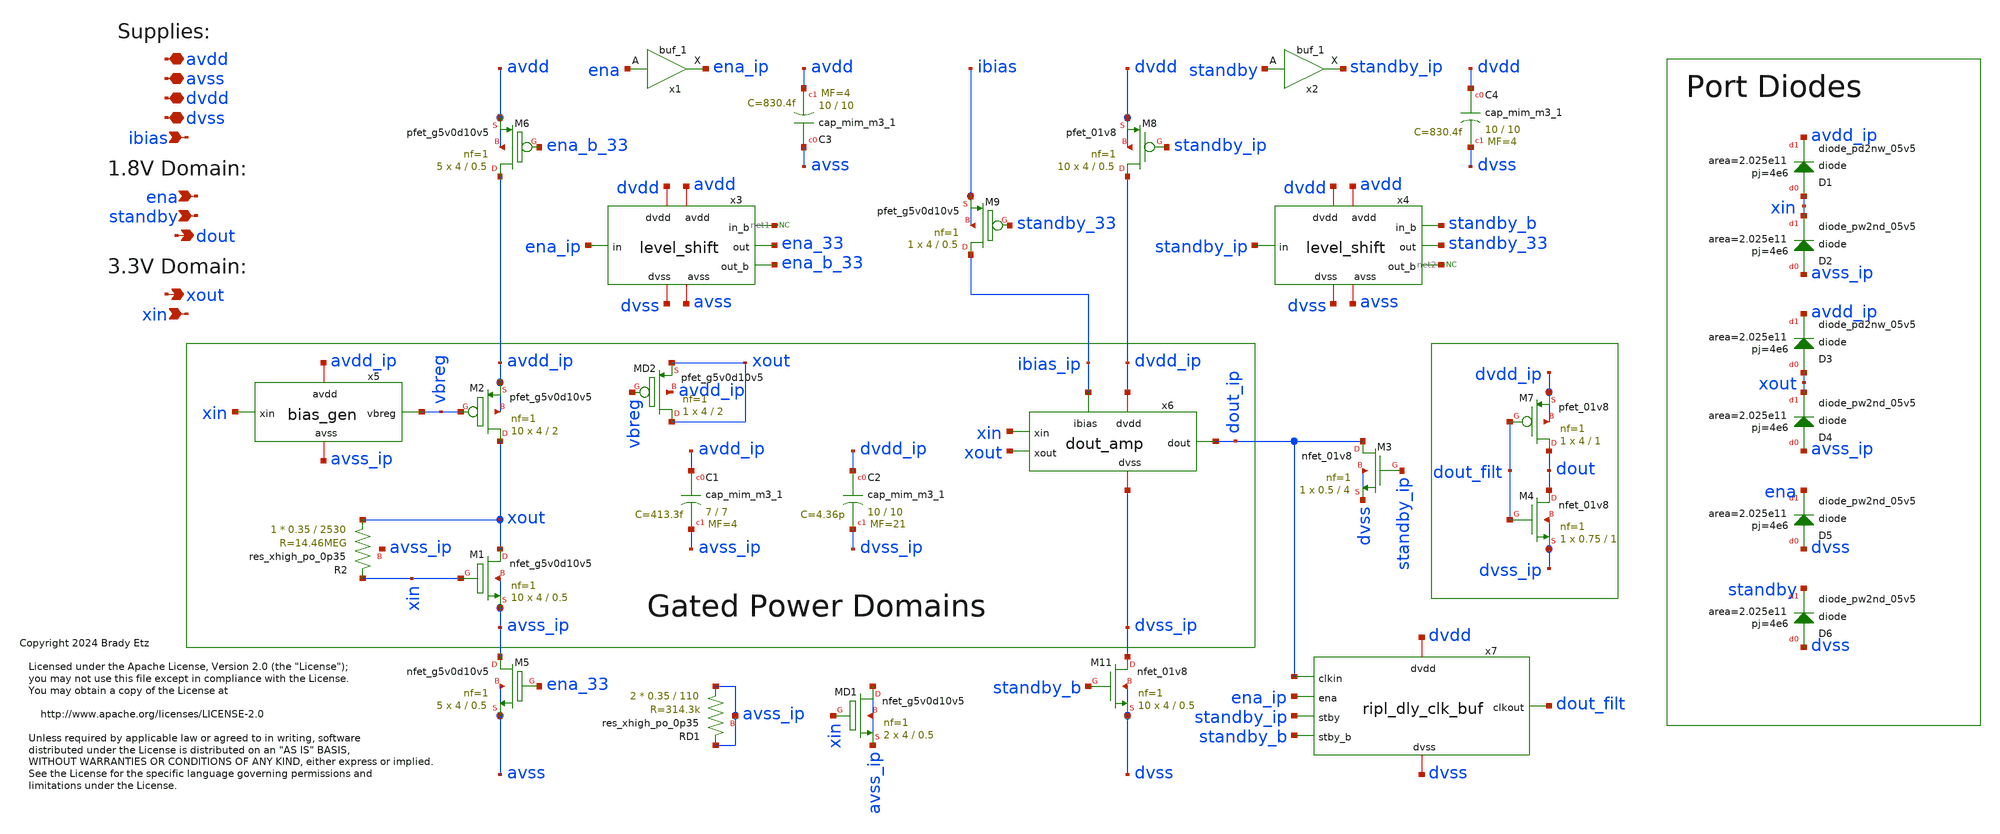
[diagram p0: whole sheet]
** sch_path: xschem/sky130_be_ip__lsxo.sch
* Copyright 2024 Brady Etz
* Licensed under the Apache License, Version 2.0 (the "License");
**.subckt sky130_be_ip__lsxo avdd dout avss dvdd dvss ibias ena standby xin xout
*.iopin avdd
*.opin dout
*.iopin avss
*.iopin dvdd
*.iopin dvss
*.ipin ibias
*.ipin ena
*.ipin standby
*.ipin xin
*.opin xout
XM1 xout xin avss_ip avss_ip sky130_fd_pr__nfet_g5v0d10v5 L=0.5 W=4 nf=1 ad='int((nf+1)/2) * W/nf * 0.29'
+ as='int((nf+2)/2) * W/nf * 0.29' pd='2*int((nf+1)/2) * (W/nf + 0.29)' ps='2*int((nf+2)/2) * (W/nf + 0.29)'
+ nrd='0.29 / W' nrs='0.29 / W' sa=0 sb=0 sd=0 mult=10 m=10
XM2 xout vbreg avdd_ip avdd_ip sky130_fd_pr__pfet_g5v0d10v5 L=2 W=4 nf=1 ad='int((nf+1)/2) * W/nf * 0.29'
+ as='int((nf+2)/2) * W/nf * 0.29' pd='2*int((nf+1)/2) * (W/nf + 0.29)' ps='2*int((nf+2)/2) * (W/nf + 0.29)'
+ nrd='0.29 / W' nrs='0.29 / W' sa=0 sb=0 sd=0 mult=10 m=10
XR2 xout xin avss_ip sky130_fd_pr__res_xhigh_po_0p35 L=2530 mult=1 m=1
XM5 avss_ip ena_33 avss avss sky130_fd_pr__nfet_g5v0d10v5 L=0.5 W=4 nf=1 ad='int((nf+1)/2) * W/nf * 0.29'
+ as='int((nf+2)/2) * W/nf * 0.29' pd='2*int((nf+1)/2) * (W/nf + 0.29)' ps='2*int((nf+2)/2) * (W/nf + 0.29)'
+ nrd='0.29 / W' nrs='0.29 / W' sa=0 sb=0 sd=0 mult=5 m=5
XM6 avdd_ip ena_b_33 avdd avdd sky130_fd_pr__pfet_g5v0d10v5 L=0.5 W=4 nf=1 ad='int((nf+1)/2) * W/nf * 0.29'
+ as='int((nf+2)/2) * W/nf * 0.29' pd='2*int((nf+1)/2) * (W/nf + 0.29)' ps='2*int((nf+2)/2) * (W/nf + 0.29)'
+ nrd='0.29 / W' nrs='0.29 / W' sa=0 sb=0 sd=0 mult=5 m=5
XM8 dvdd_ip standby_ip dvdd dvdd sky130_fd_pr__pfet_01v8 L=0.5 W=4 nf=1 ad='int((nf+1)/2) * W/nf * 0.29'
+ as='int((nf+2)/2) * W/nf * 0.29' pd='2*int((nf+1)/2) * (W/nf + 0.29)' ps='2*int((nf+2)/2) * (W/nf + 0.29)'
+ nrd='0.29 / W' nrs='0.29 / W' sa=0 sb=0 sd=0 mult=10 m=10
XM9 ibias_ip standby_33 ibias ibias sky130_fd_pr__pfet_g5v0d10v5 L=0.5 W=4 nf=1 ad='int((nf+1)/2) * W/nf * 0.29'
+ as='int((nf+2)/2) * W/nf * 0.29' pd='2*int((nf+1)/2) * (W/nf + 0.29)' ps='2*int((nf+2)/2) * (W/nf + 0.29)'
+ nrd='0.29 / W' nrs='0.29 / W' sa=0 sb=0 sd=0 mult=1 m=1
XM11 dvss_ip standby_b dvss dvss sky130_fd_pr__nfet_01v8 L=0.5 W=4 nf=1 ad='int((nf+1)/2) * W/nf * 0.29'
+ as='int((nf+2)/2) * W/nf * 0.29' pd='2*int((nf+1)/2) * (W/nf + 0.29)' ps='2*int((nf+2)/2) * (W/nf + 0.29)'
+ nrd='0.29 / W' nrs='0.29 / W' sa=0 sb=0 sd=0 mult=10 m=10
XC1 avdd_ip avss_ip sky130_fd_pr__cap_mim_m3_1 W=7 L=7 MF=4 m=4
XC2 dvdd_ip dvss_ip sky130_fd_pr__cap_mim_m3_1 W=10 L=10 MF=21 m=21
XC3 avss avdd sky130_fd_pr__cap_mim_m3_1 W=10 L=10 MF=4 m=4
XC4 dvdd dvss sky130_fd_pr__cap_mim_m3_1 W=10 L=10 MF=4 m=4
x7 dvdd dvss dout_ip dout_filt ena_ip standby_ip standby_b ripl_dly_clk_buf
XM3 dout_ip standby_ip dvss dvss sky130_fd_pr__nfet_01v8 L=4 W=0.5 nf=1 ad='int((nf+1)/2) * W/nf * 0.29'
+ as='int((nf+2)/2) * W/nf * 0.29' pd='2*int((nf+1)/2) * (W/nf + 0.29)' ps='2*int((nf+2)/2) * (W/nf + 0.29)'
+ nrd='0.29 / W' nrs='0.29 / W' sa=0 sb=0 sd=0 mult=1 m=1
x3 avdd dvdd ena_33 ena_b_33 ena_ip dvss avss net1 level_shift
x4 avdd dvdd standby_33 net2 standby_ip dvss avss standby_b level_shift
x6 dvdd_ip dvss_ip xin xout ibias_ip dout_ip dout_amp
x5 avdd_ip vbreg xin avss_ip bias_gen
XM4 dout dout_filt dvss_ip dvss_ip sky130_fd_pr__nfet_01v8 L=1 W=0.75 nf=1 ad='int((nf+1)/2) * W/nf * 0.29'
+ as='int((nf+2)/2) * W/nf * 0.29' pd='2*int((nf+1)/2) * (W/nf + 0.29)' ps='2*int((nf+2)/2) * (W/nf + 0.29)'
+ nrd='0.29 / W' nrs='0.29 / W' sa=0 sb=0 sd=0 mult=1 m=1
XM7 dout dout_filt dvdd_ip dvdd_ip sky130_fd_pr__pfet_01v8 L=1 W=4 nf=1 ad='int((nf+1)/2) * W/nf * 0.29'
+ as='int((nf+2)/2) * W/nf * 0.29' pd='2*int((nf+1)/2) * (W/nf + 0.29)' ps='2*int((nf+2)/2) * (W/nf + 0.29)'
+ nrd='0.29 / W' nrs='0.29 / W' sa=0 sb=0 sd=0 mult=1 m=1
x1 ena dvss dvss dvdd dvdd ena_ip sky130_fd_sc_hd__buf_1
x2 standby dvss dvss dvdd dvdd standby_ip sky130_fd_sc_hd__buf_1
* noconn #net1
* noconn #net2
XRD1 avss_ip avss_ip avss_ip sky130_fd_pr__res_xhigh_po_0p35 L=110 mult=2 m=2
XMD1 avss_ip xin avss_ip avss_ip sky130_fd_pr__nfet_g5v0d10v5 L=0.5 W=4 nf=1 ad='int((nf+1)/2) * W/nf * 0.29'
+ as='int((nf+2)/2) * W/nf * 0.29' pd='2*int((nf+1)/2) * (W/nf + 0.29)' ps='2*int((nf+2)/2) * (W/nf + 0.29)'
+ nrd='0.29 / W' nrs='0.29 / W' sa=0 sb=0 sd=0 mult=2 m=2
XD1 xin avdd_ip sky130_fd_pr__diode_pd2nw_05v5 area=2.025e11 pj=4e6
XD2 avss_ip xin sky130_fd_pr__diode_pw2nd_05v5 area=2.025e11 pj=4e6
XD3 xout avdd_ip sky130_fd_pr__diode_pd2nw_05v5 area=2.025e11 pj=4e6
XD4 avss_ip xout sky130_fd_pr__diode_pw2nd_05v5 area=2.025e11 pj=4e6
XD5 dvss ena sky130_fd_pr__diode_pw2nd_05v5 area=2.025e11 pj=4e6
XD6 dvss standby sky130_fd_pr__diode_pw2nd_05v5 area=2.025e11 pj=4e6
XMD2 xout vbreg xout avdd_ip sky130_fd_pr__pfet_g5v0d10v5 L=2 W=4 nf=1 ad='int((nf+1)/2) * W/nf * 0.29'
+ as='int((nf+2)/2) * W/nf * 0.29' pd='2*int((nf+1)/2) * (W/nf + 0.29)' ps='2*int((nf+2)/2) * (W/nf + 0.29)'
+ nrd='0.29 / W' nrs='0.29 / W' sa=0 sb=0 sd=0 mult=1 m=1
**.ends

* expanding   symbol:  ripl_dly_clk_buf.sym # of pins=7
** sym_path: xschem/ripl_dly_clk_buf.sym
** sch_path: xschem/ripl_dly_clk_buf.sch
.subckt ripl_dly_clk_buf dvdd dvss clkin clkout ena stby stby_b
*.iopin dvdd
*.iopin dvss
*.ipin clkin
*.opin clkout
*.ipin ena
*.ipin stby
*.ipin stby_b
XM3 clkout clk_disable dvss dvss sky130_fd_pr__nfet_01v8 L=4 W=0.5 nf=1 ad='int((nf+1)/2) * W/nf * 0.29'
+ as='int((nf+2)/2) * W/nf * 0.29' pd='2*int((nf+1)/2) * (W/nf + 0.29)' ps='2*int((nf+2)/2) * (W/nf + 0.29)'
+ nrd='0.29 / W' nrs='0.29 / W' sa=0 sb=0 sd=0 mult=1 m=1
x3 stby_b stby_done_b ena ena_done_b stby dvss dvss dvdd dvdd clk_disable sky130_fd_sc_hd__a221o_1
x2 dvdd dvss clkin stby_done_b stby_b ripple_dly_4
x1 dvdd dvss clkin ena_done_b ena ripple_dly_4
x5 clkin clk_disable dvss dvss dvdd dvdd clkout sky130_fd_sc_hd__einvn_0
.ends


* expanding   symbol:  level_shift.sym # of pins=8
** sym_path: xschem/level_shift.sym
** sch_path: xschem/level_shift.sch
.subckt level_shift avdd dvdd out out_b in dvss avss in_b
*.ipin in
*.iopin avdd
*.iopin avss
*.iopin dvss
*.iopin dvdd
*.opin out
*.opin out_b
*.opin in_b
XM4 out in_b avss avss sky130_fd_pr__nfet_g5v0d10v5 L=0.5 W=3 nf=1 ad='int((nf+1)/2) * W/nf * 0.29' as='int((nf+2)/2) * W/nf * 0.29'
+ pd='2*int((nf+1)/2) * (W/nf + 0.29)' ps='2*int((nf+2)/2) * (W/nf + 0.29)' nrd='0.29 / W' nrs='0.29 / W'
+ sa=0 sb=0 sd=0 mult=2 m=2
XM3 out_b in avss avss sky130_fd_pr__nfet_g5v0d10v5 L=0.5 W=3 nf=1 ad='int((nf+1)/2) * W/nf * 0.29' as='int((nf+2)/2) * W/nf * 0.29'
+ pd='2*int((nf+1)/2) * (W/nf + 0.29)' ps='2*int((nf+2)/2) * (W/nf + 0.29)' nrd='0.29 / W' nrs='0.29 / W'
+ sa=0 sb=0 sd=0 mult=2 m=2
XM5 out_b out avdd avdd sky130_fd_pr__pfet_g5v0d10v5 L=4 W=1 nf=1 ad='int((nf+1)/2) * W/nf * 0.29' as='int((nf+2)/2) * W/nf * 0.29'
+ pd='2*int((nf+1)/2) * (W/nf + 0.29)' ps='2*int((nf+2)/2) * (W/nf + 0.29)' nrd='0.29 / W' nrs='0.29 / W'
+ sa=0 sb=0 sd=0 mult=1 m=1
XM6 out out_b avdd avdd sky130_fd_pr__pfet_g5v0d10v5 L=4 W=1 nf=1 ad='int((nf+1)/2) * W/nf * 0.29' as='int((nf+2)/2) * W/nf * 0.29'
+ pd='2*int((nf+1)/2) * (W/nf + 0.29)' ps='2*int((nf+2)/2) * (W/nf + 0.29)' nrd='0.29 / W' nrs='0.29 / W'
+ sa=0 sb=0 sd=0 mult=1 m=1
XM2 in_b in dvdd dvdd sky130_fd_pr__pfet_01v8 L=1 W=1 nf=1 ad='int((nf+1)/2) * W/nf * 0.29' as='int((nf+2)/2) * W/nf * 0.29'
+ pd='2*int((nf+1)/2) * (W/nf + 0.29)' ps='2*int((nf+2)/2) * (W/nf + 0.29)' nrd='0.29 / W' nrs='0.29 / W'
+ sa=0 sb=0 sd=0 mult=1 m=1
XM1 in_b in dvss dvss sky130_fd_pr__nfet_01v8 L=1 W=1 nf=1 ad='int((nf+1)/2) * W/nf * 0.29' as='int((nf+2)/2) * W/nf * 0.29'
+ pd='2*int((nf+1)/2) * (W/nf + 0.29)' ps='2*int((nf+2)/2) * (W/nf + 0.29)' nrd='0.29 / W' nrs='0.29 / W'
+ sa=0 sb=0 sd=0 mult=1 m=1
.ends


* expanding   symbol:  dout_amp.sym # of pins=6
** sym_path: xschem/dout_amp.sym
** sch_path: xschem/dout_amp.sch
.subckt dout_amp dvdd dvss xin xout ibias dout
*.ipin xin
*.iopin dvdd
*.iopin dvss
*.opin dout
*.ipin ibias
*.ipin xout
XM1 ibias ibias dvss dvss sky130_fd_pr__nfet_g5v0d10v5 L=2 W=2 nf=1 ad='int((nf+1)/2) * W/nf * 0.29'
+ as='int((nf+2)/2) * W/nf * 0.29' pd='2*int((nf+1)/2) * (W/nf + 0.29)' ps='2*int((nf+2)/2) * (W/nf + 0.29)'
+ nrd='0.29 / W' nrs='0.29 / W' sa=0 sb=0 sd=0 mult=5 m=5
XM2 vbp ibias dvss dvss sky130_fd_pr__nfet_g5v0d10v5 L=2 W=2 nf=1 ad='int((nf+1)/2) * W/nf * 0.29' as='int((nf+2)/2) * W/nf * 0.29'
+ pd='2*int((nf+1)/2) * (W/nf + 0.29)' ps='2*int((nf+2)/2) * (W/nf + 0.29)' nrd='0.29 / W' nrs='0.29 / W'
+ sa=0 sb=0 sd=0 mult=1 m=1
XM5 vn xin tail dvdd sky130_fd_pr__pfet_g5v0d10v5 L=2 W=4 nf=1 ad='int((nf+1)/2) * W/nf * 0.29' as='int((nf+2)/2) * W/nf * 0.29'
+ pd='2*int((nf+1)/2) * (W/nf + 0.29)' ps='2*int((nf+2)/2) * (W/nf + 0.29)' nrd='0.29 / W' nrs='0.29 / W'
+ sa=0 sb=0 sd=0 mult=1 m=1
XC1 inv_in xin_buf sky130_fd_pr__cap_mim_m3_1 W=10 L=10 MF=12 m=12
XM6 inv_m1 inv_in dvdd dvdd sky130_fd_pr__pfet_01v8 L=8 W=0.5 nf=1 ad='int((nf+1)/2) * W/nf * 0.29' as='int((nf+2)/2) * W/nf * 0.29'
+ pd='2*int((nf+1)/2) * (W/nf + 0.29)' ps='2*int((nf+2)/2) * (W/nf + 0.29)' nrd='0.29 / W' nrs='0.29 / W'
+ sa=0 sb=0 sd=0 mult=1 m=1
XM7 inv_m1 inv_in dvss dvss sky130_fd_pr__nfet_01v8 L=8 W=0.5 nf=1 ad='int((nf+1)/2) * W/nf * 0.29' as='int((nf+2)/2) * W/nf * 0.29'
+ pd='2*int((nf+1)/2) * (W/nf + 0.29)' ps='2*int((nf+2)/2) * (W/nf + 0.29)' nrd='0.29 / W' nrs='0.29 / W'
+ sa=0 sb=0 sd=0 mult=1 m=1
XM8 net1 net1 dvdd dvdd sky130_fd_pr__pfet_01v8 L=8 W=0.5 nf=1 ad='int((nf+1)/2) * W/nf * 0.29' as='int((nf+2)/2) * W/nf * 0.29'
+ pd='2*int((nf+1)/2) * (W/nf + 0.29)' ps='2*int((nf+2)/2) * (W/nf + 0.29)' nrd='0.29 / W' nrs='0.29 / W'
+ sa=0 sb=0 sd=0 mult=1 m=1
XM9 net1 net1 dvss dvss sky130_fd_pr__nfet_01v8 L=8 W=0.5 nf=1 ad='int((nf+1)/2) * W/nf * 0.29' as='int((nf+2)/2) * W/nf * 0.29'
+ pd='2*int((nf+1)/2) * (W/nf + 0.29)' ps='2*int((nf+2)/2) * (W/nf + 0.29)' nrd='0.29 / W' nrs='0.29 / W'
+ sa=0 sb=0 sd=0 mult=1 m=1
XR1 inv_in net1 dvss sky130_fd_pr__res_xhigh_po_0p35 L=990 mult=1 m=1
XM10 inv_m2 inv_m1 dvdd dvdd sky130_fd_pr__pfet_01v8 L=1 W=0.5 nf=1 ad='int((nf+1)/2) * W/nf * 0.29'
+ as='int((nf+2)/2) * W/nf * 0.29' pd='2*int((nf+1)/2) * (W/nf + 0.29)' ps='2*int((nf+2)/2) * (W/nf + 0.29)'
+ nrd='0.29 / W' nrs='0.29 / W' sa=0 sb=0 sd=0 mult=1 m=1
XM11 inv_m2 inv_m1 dvss dvss sky130_fd_pr__nfet_01v8 L=1 W=0.5 nf=1 ad='int((nf+1)/2) * W/nf * 0.29'
+ as='int((nf+2)/2) * W/nf * 0.29' pd='2*int((nf+1)/2) * (W/nf + 0.29)' ps='2*int((nf+2)/2) * (W/nf + 0.29)'
+ nrd='0.29 / W' nrs='0.29 / W' sa=0 sb=0 sd=0 mult=1 m=1
XM12 dout inv_m2 dvdd dvdd sky130_fd_pr__pfet_01v8 L=1 W=0.5 nf=1 ad='int((nf+1)/2) * W/nf * 0.29' as='int((nf+2)/2) * W/nf * 0.29'
+ pd='2*int((nf+1)/2) * (W/nf + 0.29)' ps='2*int((nf+2)/2) * (W/nf + 0.29)' nrd='0.29 / W' nrs='0.29 / W'
+ sa=0 sb=0 sd=0 mult=2 m=2
XM13 dout inv_m2 dvss dvss sky130_fd_pr__nfet_01v8 L=1 W=0.5 nf=1 ad='int((nf+1)/2) * W/nf * 0.29' as='int((nf+2)/2) * W/nf * 0.29'
+ pd='2*int((nf+1)/2) * (W/nf + 0.29)' ps='2*int((nf+2)/2) * (W/nf + 0.29)' nrd='0.29 / W' nrs='0.29 / W'
+ sa=0 sb=0 sd=0 mult=2 m=2
XM16 tail vbp dvdd dvdd sky130_fd_pr__pfet_01v8 L=2 W=2 nf=1 ad='int((nf+1)/2) * W/nf * 0.29' as='int((nf+2)/2) * W/nf * 0.29'
+ pd='2*int((nf+1)/2) * (W/nf + 0.29)' ps='2*int((nf+2)/2) * (W/nf + 0.29)' nrd='0.29 / W' nrs='0.29 / W'
+ sa=0 sb=0 sd=0 mult=10 m=10
XM17 vbp vbp dvdd dvdd sky130_fd_pr__pfet_01v8 L=2 W=2 nf=1 ad='int((nf+1)/2) * W/nf * 0.29' as='int((nf+2)/2) * W/nf * 0.29'
+ pd='2*int((nf+1)/2) * (W/nf + 0.29)' ps='2*int((nf+2)/2) * (W/nf + 0.29)' nrd='0.29 / W' nrs='0.29 / W'
+ sa=0 sb=0 sd=0 mult=1 m=1
XM3 xin_buf xout tail dvdd sky130_fd_pr__pfet_g5v0d10v5 L=2 W=4 nf=1 ad='int((nf+1)/2) * W/nf * 0.29'
+ as='int((nf+2)/2) * W/nf * 0.29' pd='2*int((nf+1)/2) * (W/nf + 0.29)' ps='2*int((nf+2)/2) * (W/nf + 0.29)'
+ nrd='0.29 / W' nrs='0.29 / W' sa=0 sb=0 sd=0 mult=1 m=1
XM4 xin_buf vn dvss dvss sky130_fd_pr__nfet_01v8 L=2 W=4 nf=1 ad='int((nf+1)/2) * W/nf * 0.29' as='int((nf+2)/2) * W/nf * 0.29'
+ pd='2*int((nf+1)/2) * (W/nf + 0.29)' ps='2*int((nf+2)/2) * (W/nf + 0.29)' nrd='0.29 / W' nrs='0.29 / W'
+ sa=0 sb=0 sd=0 mult=1 m=1
XM18 vn vn dvss dvss sky130_fd_pr__nfet_01v8 L=2 W=4 nf=1 ad='int((nf+1)/2) * W/nf * 0.29' as='int((nf+2)/2) * W/nf * 0.29'
+ pd='2*int((nf+1)/2) * (W/nf + 0.29)' ps='2*int((nf+2)/2) * (W/nf + 0.29)' nrd='0.29 / W' nrs='0.29 / W'
+ sa=0 sb=0 sd=0 mult=1 m=1
XMD2 vn vn vn dvss sky130_fd_pr__nfet_01v8 L=2 W=4 nf=1 ad='int((nf+1)/2) * W/nf * 0.29' as='int((nf+2)/2) * W/nf * 0.29'
+ pd='2*int((nf+1)/2) * (W/nf + 0.29)' ps='2*int((nf+2)/2) * (W/nf + 0.29)' nrd='0.29 / W' nrs='0.29 / W'
+ sa=0 sb=0 sd=0 mult=1 m=1
XMD1 dvdd inv_m1 dvdd dvdd sky130_fd_pr__pfet_01v8 L=1 W=0.5 nf=1 ad='int((nf+1)/2) * W/nf * 0.29' as='int((nf+2)/2) * W/nf * 0.29'
+ pd='2*int((nf+1)/2) * (W/nf + 0.29)' ps='2*int((nf+2)/2) * (W/nf + 0.29)' nrd='0.29 / W' nrs='0.29 / W'
+ sa=0 sb=0 sd=0 mult=1 m=1
XMD4 dvss ibias dvss dvss sky130_fd_pr__nfet_g5v0d10v5 L=2 W=2 nf=1 ad='int((nf+1)/2) * W/nf * 0.29'
+ as='int((nf+2)/2) * W/nf * 0.29' pd='2*int((nf+1)/2) * (W/nf + 0.29)' ps='2*int((nf+2)/2) * (W/nf + 0.29)'
+ nrd='0.29 / W' nrs='0.29 / W' sa=0 sb=0 sd=0 mult=2 m=2
XMD3 dvdd vbp dvdd dvdd sky130_fd_pr__pfet_01v8 L=2 W=2 nf=1 ad='int((nf+1)/2) * W/nf * 0.29' as='int((nf+2)/2) * W/nf * 0.29'
+ pd='2*int((nf+1)/2) * (W/nf + 0.29)' ps='2*int((nf+2)/2) * (W/nf + 0.29)' nrd='0.29 / W' nrs='0.29 / W'
+ sa=0 sb=0 sd=0 mult=5 m=5
XMD5 vn xin vn dvdd sky130_fd_pr__pfet_g5v0d10v5 L=2 W=4 nf=1 ad='int((nf+1)/2) * W/nf * 0.29' as='int((nf+2)/2) * W/nf * 0.29'
+ pd='2*int((nf+1)/2) * (W/nf + 0.29)' ps='2*int((nf+2)/2) * (W/nf + 0.29)' nrd='0.29 / W' nrs='0.29 / W'
+ sa=0 sb=0 sd=0 mult=1 m=1
XMD6 xin_buf vn xin_buf dvss sky130_fd_pr__nfet_01v8 L=2 W=4 nf=1 ad='int((nf+1)/2) * W/nf * 0.29' as='int((nf+2)/2) * W/nf * 0.29'
+ pd='2*int((nf+1)/2) * (W/nf + 0.29)' ps='2*int((nf+2)/2) * (W/nf + 0.29)' nrd='0.29 / W' nrs='0.29 / W'
+ sa=0 sb=0 sd=0 mult=1 m=1
XMD7 xin_buf xout xin_buf dvdd sky130_fd_pr__pfet_g5v0d10v5 L=2 W=4 nf=1 ad='int((nf+1)/2) * W/nf * 0.29'
+ as='int((nf+2)/2) * W/nf * 0.29' pd='2*int((nf+1)/2) * (W/nf + 0.29)' ps='2*int((nf+2)/2) * (W/nf + 0.29)'
+ nrd='0.29 / W' nrs='0.29 / W' sa=0 sb=0 sd=0 mult=1 m=1
XMD8 dvss inv_m1 dvss dvss sky130_fd_pr__nfet_01v8 L=1 W=0.5 nf=1 ad='int((nf+1)/2) * W/nf * 0.29' as='int((nf+2)/2) * W/nf * 0.29'
+ pd='2*int((nf+1)/2) * (W/nf + 0.29)' ps='2*int((nf+2)/2) * (W/nf + 0.29)' nrd='0.29 / W' nrs='0.29 / W'
+ sa=0 sb=0 sd=0 mult=1 m=1
.ends


* expanding   symbol:  bias_gen.sym # of pins=4
** sym_path: xschem/bias_gen.sym
** sch_path: xschem/bias_gen.sch
.subckt bias_gen avdd vbreg xin avss
*.ipin xin
*.iopin avdd
*.iopin avss
*.opin vbreg
XM2 vbreg vg2 vrb avss sky130_fd_pr__nfet_g5v0d10v5 L=2 W=4 nf=1 ad='int((nf+1)/2) * W/nf * 0.29' as='int((nf+2)/2) * W/nf * 0.29'
+ pd='2*int((nf+1)/2) * (W/nf + 0.29)' ps='2*int((nf+2)/2) * (W/nf + 0.29)' nrd='0.29 / W' nrs='0.29 / W'
+ sa=0 sb=0 sd=0 mult=4 m=4
XM3 vbreg vbreg avdd avdd sky130_fd_pr__pfet_g5v0d10v5 L=2 W=4 nf=1 ad='int((nf+1)/2) * W/nf * 0.29'
+ as='int((nf+2)/2) * W/nf * 0.29' pd='2*int((nf+1)/2) * (W/nf + 0.29)' ps='2*int((nf+2)/2) * (W/nf + 0.29)'
+ nrd='0.29 / W' nrs='0.29 / W' sa=0 sb=0 sd=0 mult=1 m=1
XM4 vg1 vbreg avdd avdd sky130_fd_pr__pfet_g5v0d10v5 L=2 W=4 nf=1 ad='int((nf+1)/2) * W/nf * 0.29' as='int((nf+2)/2) * W/nf * 0.29'
+ pd='2*int((nf+1)/2) * (W/nf + 0.29)' ps='2*int((nf+2)/2) * (W/nf + 0.29)' nrd='0.29 / W' nrs='0.29 / W'
+ sa=0 sb=0 sd=0 mult=1 m=1
XM1 vg1 vg1 avss avss sky130_fd_pr__nfet_g5v0d10v5 L=2 W=4 nf=1 ad='int((nf+1)/2) * W/nf * 0.29' as='int((nf+2)/2) * W/nf * 0.29'
+ pd='2*int((nf+1)/2) * (W/nf + 0.29)' ps='2*int((nf+2)/2) * (W/nf + 0.29)' nrd='0.29 / W' nrs='0.29 / W'
+ sa=0 sb=0 sd=0 mult=1 m=1
XR2 vg2 vg1 avss sky130_fd_pr__res_xhigh_po_0p35 L=1968 mult=1 m=1
XR3 avss vrb avss sky130_fd_pr__res_xhigh_po_0p35 L=150 mult=1 m=1
XC3 avss vg2 sky130_fd_pr__cap_mim_m3_1 W=18 L=18 MF=4 m=4
XC1 vg1 xin sky130_fd_pr__cap_mim_m3_1 W=22 L=22 MF=5 m=5
XM5 icnode vg2 avss avss sky130_fd_pr__nfet_g5v0d10v5 L=1 W=1 nf=1 ad='int((nf+1)/2) * W/nf * 0.29' as='int((nf+2)/2) * W/nf * 0.29'
+ pd='2*int((nf+1)/2) * (W/nf + 0.29)' ps='2*int((nf+2)/2) * (W/nf + 0.29)' nrd='0.29 / W' nrs='0.29 / W'
+ sa=0 sb=0 sd=0 mult=1 m=1
XC2 avdd icnode sky130_fd_pr__cap_mim_m3_1 W=20 L=20 MF=1 m=1
XM6 vbreg icnode net3 avss sky130_fd_pr__nfet_g5v0d10v5 L=8 W=0.42 nf=1 ad='int((nf+1)/2) * W/nf * 0.29'
+ as='int((nf+2)/2) * W/nf * 0.29' pd='2*int((nf+1)/2) * (W/nf + 0.29)' ps='2*int((nf+2)/2) * (W/nf + 0.29)'
+ nrd='0.29 / W' nrs='0.29 / W' sa=0 sb=0 sd=0 mult=1 m=1
XM8 net1 net1 avss avss sky130_fd_pr__nfet_g5v0d10v5 L=8 W=0.42 nf=1 ad='int((nf+1)/2) * W/nf * 0.29'
+ as='int((nf+2)/2) * W/nf * 0.29' pd='2*int((nf+1)/2) * (W/nf + 0.29)' ps='2*int((nf+2)/2) * (W/nf + 0.29)'
+ nrd='0.29 / W' nrs='0.29 / W' sa=0 sb=0 sd=0 mult=1 m=1
XM7 net3 icnode net1 avss sky130_fd_pr__nfet_g5v0d10v5 L=8 W=0.42 nf=1 ad='int((nf+1)/2) * W/nf * 0.29'
+ as='int((nf+2)/2) * W/nf * 0.29' pd='2*int((nf+1)/2) * (W/nf + 0.29)' ps='2*int((nf+2)/2) * (W/nf + 0.29)'
+ nrd='0.29 / W' nrs='0.29 / W' sa=0 sb=0 sd=0 mult=1 m=1
XRD1 avss avss avss sky130_fd_pr__res_xhigh_po_0p35 L=82 mult=2 m=2
XRD2 avss avss avss sky130_fd_pr__res_xhigh_po_0p35 L=75 mult=2 m=2
XMD1 avdd vbreg avdd avdd sky130_fd_pr__pfet_g5v0d10v5 L=2 W=4 nf=1 ad='int((nf+1)/2) * W/nf * 0.29'
+ as='int((nf+2)/2) * W/nf * 0.29' pd='2*int((nf+1)/2) * (W/nf + 0.29)' ps='2*int((nf+2)/2) * (W/nf + 0.29)'
+ nrd='0.29 / W' nrs='0.29 / W' sa=0 sb=0 sd=0 mult=4 m=4
XMD2 net2 vbreg net2 avdd sky130_fd_pr__pfet_g5v0d10v5 L=2 W=4 nf=1 ad='int((nf+1)/2) * W/nf * 0.29'
+ as='int((nf+2)/2) * W/nf * 0.29' pd='2*int((nf+1)/2) * (W/nf + 0.29)' ps='2*int((nf+2)/2) * (W/nf + 0.29)'
+ nrd='0.29 / W' nrs='0.29 / W' sa=0 sb=0 sd=0 mult=1 m=1
XMD3 avss avss avss avss sky130_fd_pr__nfet_g5v0d10v5 L=2 W=4 nf=1 ad='int((nf+1)/2) * W/nf * 0.29' as='int((nf+2)/2) * W/nf * 0.29'
+ pd='2*int((nf+1)/2) * (W/nf + 0.29)' ps='2*int((nf+2)/2) * (W/nf + 0.29)' nrd='0.29 / W' nrs='0.29 / W'
+ sa=0 sb=0 sd=0 mult=4 m=4
XMD4 vbreg vg1 vbreg avss sky130_fd_pr__nfet_g5v0d10v5 L=2 W=4 nf=1 ad='int((nf+1)/2) * W/nf * 0.29'
+ as='int((nf+2)/2) * W/nf * 0.29' pd='2*int((nf+1)/2) * (W/nf + 0.29)' ps='2*int((nf+2)/2) * (W/nf + 0.29)'
+ nrd='0.29 / W' nrs='0.29 / W' sa=0 sb=0 sd=0 mult=1 m=1
.ends


* expanding   symbol:  ripple_dly_4.sym # of pins=5
** sym_path: xschem/ripple_dly_4.sym
** sch_path: xschem/ripple_dly_4.sch
.subckt ripple_dly_4 dvdd dvss clkin doneb ena
*.ipin clkin
*.ipin ena
*.opin doneb
*.iopin dvdd
*.iopin dvss
x2 gated_clk Qb1 ena dvss dvss dvdd dvdd net1 Qb1 sky130_fd_sc_hd__dfrbp_1
x3 Qb1 Qb2 ena dvss dvss dvdd dvdd net2 Qb2 sky130_fd_sc_hd__dfrbp_1
* noconn #net1
* noconn #net2
x4 Qb2 doneb ena dvss dvss dvdd dvdd net3 doneb sky130_fd_sc_hd__dfrbp_1
x1 clkin doneb dvss dvss dvdd dvdd gated_clk sky130_fd_sc_hd__and2_0
* noconn #net3
.ends

.end
